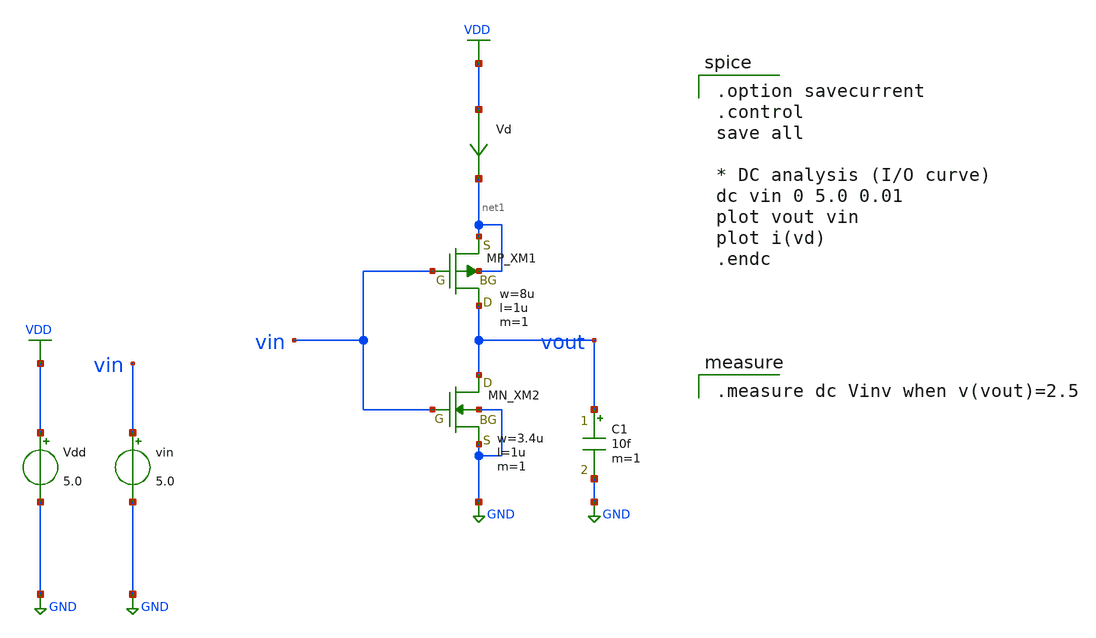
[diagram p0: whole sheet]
** sch_path: member_project/inverter/RISE-A/0x837c/inverter_sim.sch
**.subckt inverter_sim
XXM1 vout vin net1 net1 PMOS w=8u l=1u nrd=0 nrs=0 m=1
XXM2 vout vin GND GND NMOS w=3.4u l=1u nrd=0 nrs=0 m=1
Vdd VDD GND 5.0
vin vin GND 5.0
Vd VDD net1 0
.save i(vd)
C1 vout GND 10f m=1
**** begin user architecture code
 .include $::LIB/ip62_models

.option savecurrent
.control
save all

* DC analysis (I/O curve)
dc vin 0 5.0 0.01
plot vout vin
plot i(vd)
.endc


.measure dc Vinv when v(vout)=2.5

**** end user architecture code
**.ends
.GLOBAL VDD
.GLOBAL GND
.end
